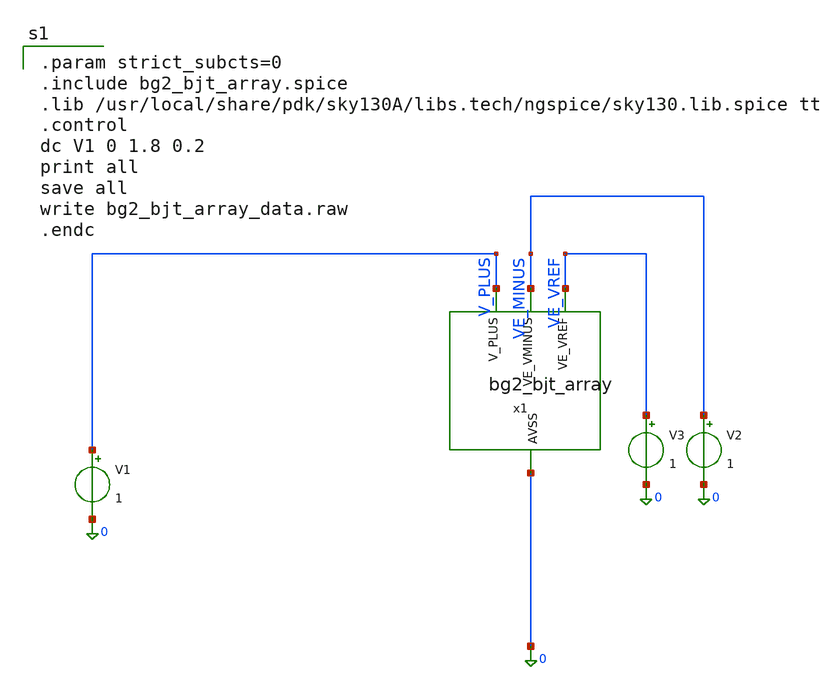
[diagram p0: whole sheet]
** sch_path: lef/lef/gds/bg2_bjt_array_tb.sch
**.subckt bg2_bjt_array_tb
V1 V_PLUS 0 1
x1 V_PLUS VE_MINUS VE_VREF 0 bg2_bjt_array
V2 VE_MINUS 0 1
V3 VE_VREF 0 1
**** begin user architecture code

.param strict_subcts=0
.include bg2_bjt_array.spice
.lib /usr/local/share/pdk/sky130A/libs.tech/ngspice/sky130.lib.spice tt
.control
dc V1 0 1.8 0.2
print all
save all
write bg2_bjt_array_data.raw
.endc

**** end user architecture code
**.ends

* expanding   symbol:  bg2_bjt_array.sym # of pins=4
** sym_path: lef/lef/gds/bg2_bjt_array.sym
** sch_path: lef/lef/gds/bg2_bjt_array.sch
.subckt bg2_bjt_array V_PLUS VE_VMINUS VE_VREF AVSS
*.ipin AVSS
*.ipin V_PLUS
*.ipin VE_VMINUS
*.ipin VE_VREF
XQ9 AVSS AVSS V_PLUS sky130_fd_pr__pnp_05v5_W3p40L3p40 m=1
XQ1 AVSS AVSS VE_VMINUS sky130_fd_pr__pnp_05v5_W3p40L3p40 m=1
XQ10 AVSS AVSS VE_VMINUS sky130_fd_pr__pnp_05v5_W3p40L3p40 m=1
XQ11 AVSS AVSS VE_VMINUS sky130_fd_pr__pnp_05v5_W3p40L3p40 m=1
XQ12 AVSS AVSS VE_VMINUS sky130_fd_pr__pnp_05v5_W3p40L3p40 m=1
XQ13 AVSS AVSS VE_VMINUS sky130_fd_pr__pnp_05v5_W3p40L3p40 m=1
XQ14 AVSS AVSS VE_VMINUS sky130_fd_pr__pnp_05v5_W3p40L3p40 m=1
XQ15 AVSS AVSS VE_VMINUS sky130_fd_pr__pnp_05v5_W3p40L3p40 m=1
XQ16 AVSS AVSS VE_VMINUS sky130_fd_pr__pnp_05v5_W3p40L3p40 m=1
XQ2 AVSS AVSS VE_VREF sky130_fd_pr__pnp_05v5_W3p40L3p40 m=1
XQ3 AVSS AVSS VE_VREF sky130_fd_pr__pnp_05v5_W3p40L3p40 m=1
XQ4 AVSS AVSS VE_VREF sky130_fd_pr__pnp_05v5_W3p40L3p40 m=1
XQ5 AVSS AVSS VE_VREF sky130_fd_pr__pnp_05v5_W3p40L3p40 m=1
XQ6 AVSS AVSS VE_VREF sky130_fd_pr__pnp_05v5_W3p40L3p40 m=1
XQ7 AVSS AVSS VE_VREF sky130_fd_pr__pnp_05v5_W3p40L3p40 m=1
XQ8 AVSS AVSS VE_VREF sky130_fd_pr__pnp_05v5_W3p40L3p40 m=1
XQ17 AVSS AVSS VE_VREF sky130_fd_pr__pnp_05v5_W3p40L3p40 m=1
XQ18 AVSS AVSS AVSS sky130_fd_pr__pnp_05v5_W3p40L3p40 m=1
XQ19 AVSS AVSS AVSS sky130_fd_pr__pnp_05v5_W3p40L3p40 m=1
XQ20 AVSS AVSS AVSS sky130_fd_pr__pnp_05v5_W3p40L3p40 m=1
XQ21 AVSS AVSS AVSS sky130_fd_pr__pnp_05v5_W3p40L3p40 m=1
XQ22 AVSS AVSS AVSS sky130_fd_pr__pnp_05v5_W3p40L3p40 m=1
XQ23 AVSS AVSS AVSS sky130_fd_pr__pnp_05v5_W3p40L3p40 m=1
XQ24 AVSS AVSS AVSS sky130_fd_pr__pnp_05v5_W3p40L3p40 m=1
XQ25 AVSS AVSS AVSS sky130_fd_pr__pnp_05v5_W3p40L3p40 m=1
XQ26 AVSS AVSS AVSS sky130_fd_pr__pnp_05v5_W3p40L3p40 m=1
XQ27 AVSS AVSS AVSS sky130_fd_pr__pnp_05v5_W3p40L3p40 m=1
XQ28 AVSS AVSS AVSS sky130_fd_pr__pnp_05v5_W3p40L3p40 m=1
XQ29 AVSS AVSS AVSS sky130_fd_pr__pnp_05v5_W3p40L3p40 m=1
XQ30 AVSS AVSS AVSS sky130_fd_pr__pnp_05v5_W3p40L3p40 m=1
XQ31 AVSS AVSS AVSS sky130_fd_pr__pnp_05v5_W3p40L3p40 m=1
XQ32 AVSS AVSS AVSS sky130_fd_pr__pnp_05v5_W3p40L3p40 m=1
XQ33 AVSS AVSS AVSS sky130_fd_pr__pnp_05v5_W3p40L3p40 m=1
XQ34 AVSS AVSS AVSS sky130_fd_pr__pnp_05v5_W3p40L3p40 m=1
XQ35 AVSS AVSS AVSS sky130_fd_pr__pnp_05v5_W3p40L3p40 m=1
XQ36 AVSS AVSS AVSS sky130_fd_pr__pnp_05v5_W3p40L3p40 m=1
XQ37 AVSS AVSS AVSS sky130_fd_pr__pnp_05v5_W3p40L3p40 m=1
XQ38 AVSS AVSS AVSS sky130_fd_pr__pnp_05v5_W3p40L3p40 m=1
XQ39 AVSS AVSS AVSS sky130_fd_pr__pnp_05v5_W3p40L3p40 m=1
XQ40 AVSS AVSS AVSS sky130_fd_pr__pnp_05v5_W3p40L3p40 m=1
XQ41 AVSS AVSS AVSS sky130_fd_pr__pnp_05v5_W3p40L3p40 m=1
XQ42 AVSS AVSS AVSS sky130_fd_pr__pnp_05v5_W3p40L3p40 m=1
XQ43 AVSS AVSS AVSS sky130_fd_pr__pnp_05v5_W3p40L3p40 m=1
XQ45 AVSS AVSS AVSS sky130_fd_pr__pnp_05v5_W3p40L3p40 m=1
.ends

.end
